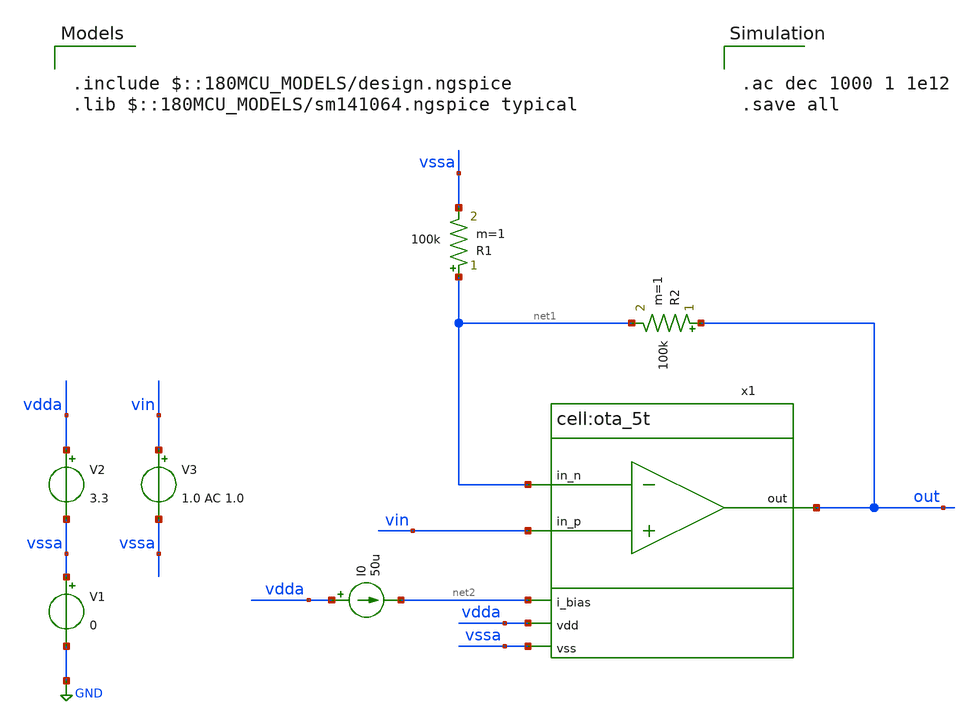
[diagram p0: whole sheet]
** sch_path: designs/libs/tb_analog/tb_ota_5t_ac/tb_ota_5t_ac.sch
**.subckt tb_ota_5t_ac
V1 vssa GND 0
V2 vdda vssa 3.3
I0 vdda net2 50u
V3 vin vssa 1.0 AC 1.0
x1 vdda out vin net1 net2 vssa ota_5t
R1 net1 vssa 100k m=1
R2 out net1 100k m=1
**** begin user architecture code


.ac dec 1000 1 1e12
.save all



.include $::180MCU_MODELS/design.ngspice
.lib $::180MCU_MODELS/sm141064.ngspice typical

**** end user architecture code
**.ends
.GLOBAL GND
.end
